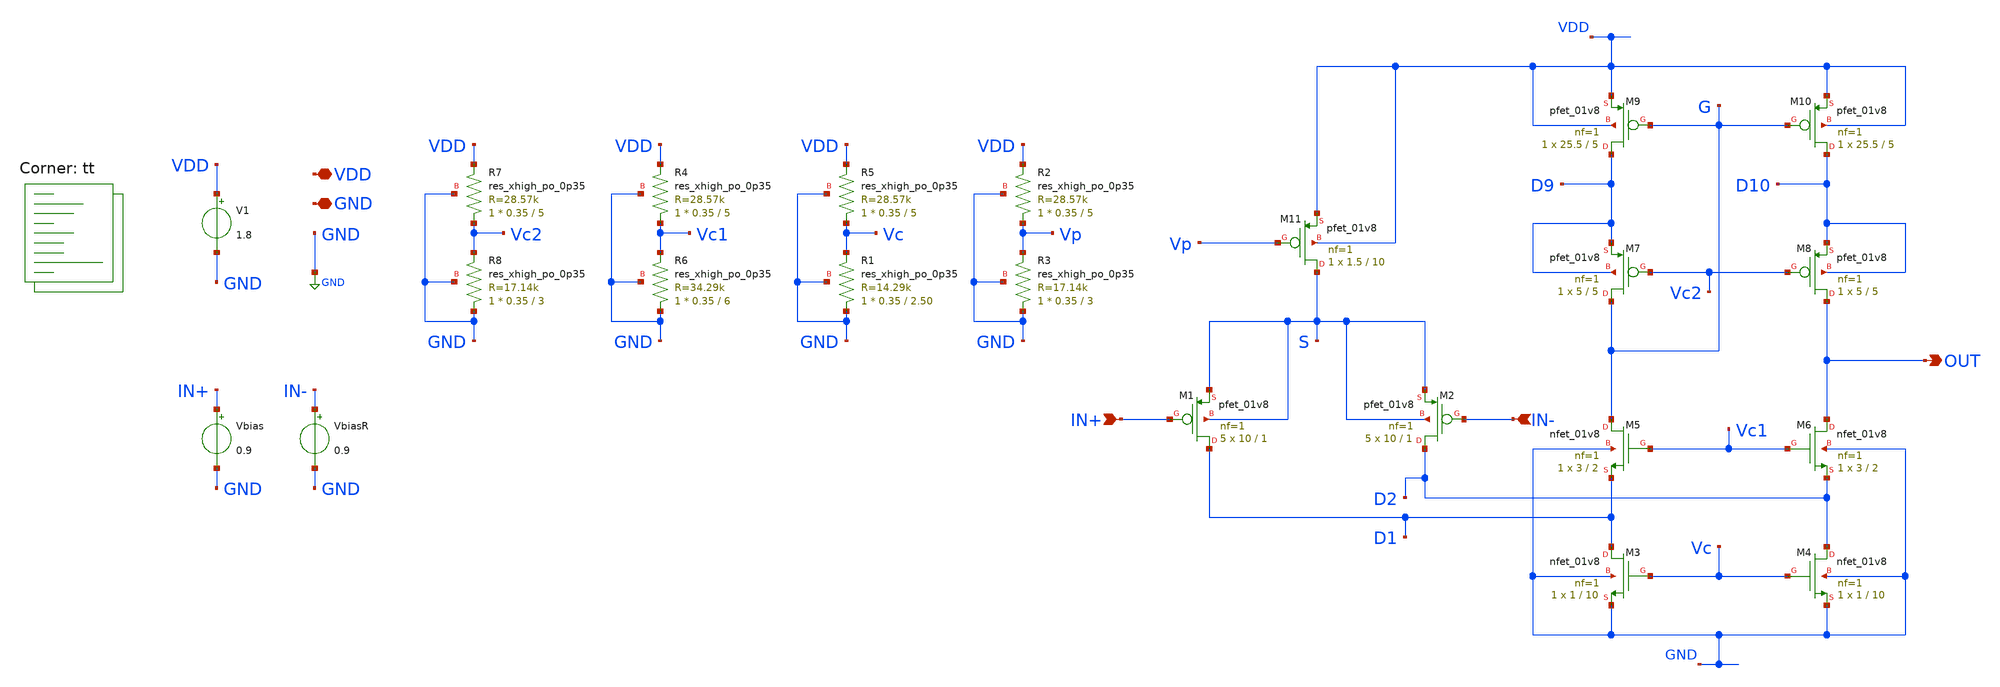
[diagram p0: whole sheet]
** sch_path: xschem/OTA_FoldedCascode0.sch
**.subckt OTA_FoldedCascode0 VDD GND IN+ IN- OUT
*.iopin VDD
*.iopin GND
*.ipin IN+
*.ipin IN-
*.opin OUT
V1 VDD GND 1.8
Vbias IN+ GND 0.9
VbiasR IN- GND 0.9
XR5 Vc VDD GND sky130_fd_pr__res_xhigh_po_0p35 L=5 mult=1 m=1
XR1 GND Vc GND sky130_fd_pr__res_xhigh_po_0p35 L=2.50 mult=1 m=1
XR2 Vp VDD GND sky130_fd_pr__res_xhigh_po_0p35 L=5 mult=1 m=1
XR3 GND Vp GND sky130_fd_pr__res_xhigh_po_0p35 L=3 mult=1 m=1
XR4 Vc1 VDD GND sky130_fd_pr__res_xhigh_po_0p35 L=5 mult=1 m=1
XR6 GND Vc1 GND sky130_fd_pr__res_xhigh_po_0p35 L=6 mult=1 m=1
XR7 Vc2 VDD GND sky130_fd_pr__res_xhigh_po_0p35 L=5 mult=1 m=1
XR8 GND Vc2 GND sky130_fd_pr__res_xhigh_po_0p35 L=3 mult=1 m=1
XM1 D1 IN+ S S sky130_fd_pr__pfet_01v8 L=1 W=10 nf=1 ad='int((nf+1)/2) * W/nf * 0.29' as='int((nf+2)/2) * W/nf * 0.29'
+ pd='2*int((nf+1)/2) * (W/nf + 0.29)' ps='2*int((nf+2)/2) * (W/nf + 0.29)' nrd='0.29 / W' nrs='0.29 / W'
+ sa=0 sb=0 sd=0 mult=5 m=5
XM2 D2 IN- S S sky130_fd_pr__pfet_01v8 L=1 W=10 nf=1 ad='int((nf+1)/2) * W/nf * 0.29' as='int((nf+2)/2) * W/nf * 0.29'
+ pd='2*int((nf+1)/2) * (W/nf + 0.29)' ps='2*int((nf+2)/2) * (W/nf + 0.29)' nrd='0.29 / W' nrs='0.29 / W'
+ sa=0 sb=0 sd=0 mult=5 m=5
XM3 D1 Vc GND GND sky130_fd_pr__nfet_01v8 L=10 W=1 nf=1 ad='int((nf+1)/2) * W/nf * 0.29' as='int((nf+2)/2) * W/nf * 0.29'
+ pd='2*int((nf+1)/2) * (W/nf + 0.29)' ps='2*int((nf+2)/2) * (W/nf + 0.29)' nrd='0.29 / W' nrs='0.29 / W'
+ sa=0 sb=0 sd=0 mult=1 m=1
XM4 D2 Vc GND GND sky130_fd_pr__nfet_01v8 L=10 W=1 nf=1 ad='int((nf+1)/2) * W/nf * 0.29' as='int((nf+2)/2) * W/nf * 0.29'
+ pd='2*int((nf+1)/2) * (W/nf + 0.29)' ps='2*int((nf+2)/2) * (W/nf + 0.29)' nrd='0.29 / W' nrs='0.29 / W'
+ sa=0 sb=0 sd=0 mult=1 m=1
XM5 G Vc1 D1 GND sky130_fd_pr__nfet_01v8 L=2 W=3 nf=1 ad='int((nf+1)/2) * W/nf * 0.29' as='int((nf+2)/2) * W/nf * 0.29'
+ pd='2*int((nf+1)/2) * (W/nf + 0.29)' ps='2*int((nf+2)/2) * (W/nf + 0.29)' nrd='0.29 / W' nrs='0.29 / W'
+ sa=0 sb=0 sd=0 mult=1 m=1
XM6 OUT Vc1 D2 GND sky130_fd_pr__nfet_01v8 L=2 W=3 nf=1 ad='int((nf+1)/2) * W/nf * 0.29' as='int((nf+2)/2) * W/nf * 0.29'
+ pd='2*int((nf+1)/2) * (W/nf + 0.29)' ps='2*int((nf+2)/2) * (W/nf + 0.29)' nrd='0.29 / W' nrs='0.29 / W'
+ sa=0 sb=0 sd=0 mult=1 m=1
XM7 G Vc2 D9 D9 sky130_fd_pr__pfet_01v8 L=5 W=5 nf=1 ad='int((nf+1)/2) * W/nf * 0.29' as='int((nf+2)/2) * W/nf * 0.29'
+ pd='2*int((nf+1)/2) * (W/nf + 0.29)' ps='2*int((nf+2)/2) * (W/nf + 0.29)' nrd='0.29 / W' nrs='0.29 / W'
+ sa=0 sb=0 sd=0 mult=1 m=1
XM8 OUT Vc2 D10 D10 sky130_fd_pr__pfet_01v8 L=5 W=5 nf=1 ad='int((nf+1)/2) * W/nf * 0.29' as='int((nf+2)/2) * W/nf * 0.29'
+ pd='2*int((nf+1)/2) * (W/nf + 0.29)' ps='2*int((nf+2)/2) * (W/nf + 0.29)' nrd='0.29 / W' nrs='0.29 / W'
+ sa=0 sb=0 sd=0 mult=1 m=1
XM9 D9 G VDD VDD sky130_fd_pr__pfet_01v8 L=5 W=25.5 nf=1 ad='int((nf+1)/2) * W/nf * 0.29' as='int((nf+2)/2) * W/nf * 0.29'
+ pd='2*int((nf+1)/2) * (W/nf + 0.29)' ps='2*int((nf+2)/2) * (W/nf + 0.29)' nrd='0.29 / W' nrs='0.29 / W'
+ sa=0 sb=0 sd=0 mult=1 m=1
XM10 D10 G VDD VDD sky130_fd_pr__pfet_01v8 L=5 W=25.5 nf=1 ad='int((nf+1)/2) * W/nf * 0.29' as='int((nf+2)/2) * W/nf * 0.29'
+ pd='2*int((nf+1)/2) * (W/nf + 0.29)' ps='2*int((nf+2)/2) * (W/nf + 0.29)' nrd='0.29 / W' nrs='0.29 / W'
+ sa=0 sb=0 sd=0 mult=1 m=1
XM11 S Vp VDD VDD sky130_fd_pr__pfet_01v8 L=10 W=1.5 nf=1 ad='int((nf+1)/2) * W / nf * 0.29' as='int((nf+2)/2) * W / nf * 0.29'
+ pd='2*int((nf+1)/2) * (W / nf + 0.29)' ps='2*int((nf+2)/2) * (W / nf + 0.29)' nrd='0.29 / W ' nrs='0.29 / W '
+ sa=0 sb=0 sd=0 mult=1 m=1
**** begin user architecture code



* ngspice commands

.options savecurrents

.control
save all
save @m.xm1.msky130_fd_pr__pfet_01v8[gm]
save @m.xm2.msky130_fd_pr__pfet_01v8[gm]
save @m.xm3.msky130_fd_pr__nfet_01v8[gm]
save @m.xm4.msky130_fd_pr__nfet_01v8[gm]
save @m.xm5.msky130_fd_pr__nfet_01v8[gm]
save @m.xm6.msky130_fd_pr__nfet_01v8[gm]
save @m.xm7.msky130_fd_pr__pfet_01v8[gm]
save @m.xm8.msky130_fd_pr__pfet_01v8[gm]
save @m.xm9.msky130_fd_pr__pfet_01v8[gm]
save @m.xm10.msky130_fd_pr__pfet_01v8[gm]

   op
   remzerovec
   write OTA_FoldedCascode0.raw
   set appendwrite
   dc Vbias 0.899 0.901 0.00001

   *dc Vbias 0 1.8 0.01
   *remzerovec
   plot v(out),v(in+)
   plot deriv(v(out))

   write OTA_FoldedCascode0.raw
.measure gain max(deriv(v(out)))
.endc
.end



.lib $::SKYWATER_MODELS/sky130.lib.spice tt
**** end user architecture code
**.ends
.GLOBAL GND
.end
